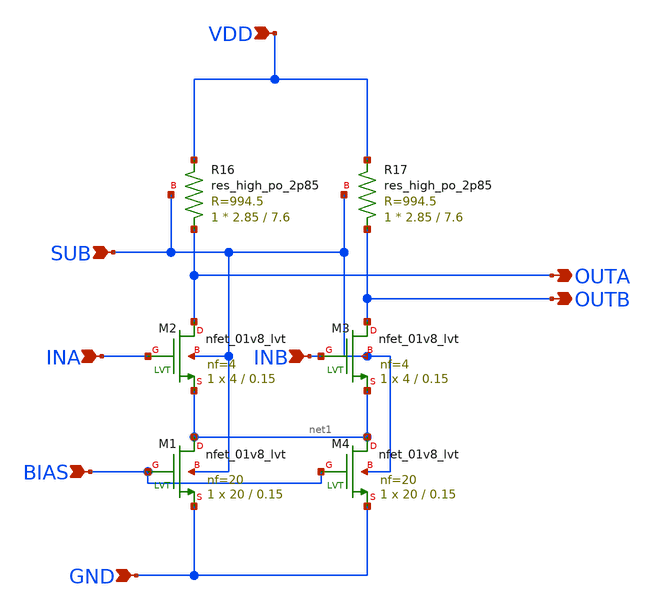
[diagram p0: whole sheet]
** sch_path: design/vco/5~10Ghiarachy_final/core_osc_amp.sch
**.subckt core_osc_amp INA INB BIAS GND VDD SUB OUTA OUTB
*.ipin INA
*.ipin INB
*.ipin BIAS
*.ipin GND
*.ipin VDD
*.ipin SUB
*.opin OUTA
*.opin OUTB
XM2 OUTA INA net1 SUB sky130_fd_pr__nfet_01v8_lvt L=0.15 W=4 nf=4 ad='int((nf+1)/2) * W/nf * 0.29' as='int((nf+2)/2) * W/nf * 0.29'
+ pd='2*int((nf+1)/2) * (W/nf + 0.29)' ps='2*int((nf+2)/2) * (W/nf + 0.29)' nrd='0.29 / W' nrs='0.29 / W'
+ sa=0 sb=0 sd=0 mult=1 m=1
XM3 OUTB INB net1 SUB sky130_fd_pr__nfet_01v8_lvt L=0.15 W=4 nf=4 ad='int((nf+1)/2) * W/nf * 0.29' as='int((nf+2)/2) * W/nf * 0.29'
+ pd='2*int((nf+1)/2) * (W/nf + 0.29)' ps='2*int((nf+2)/2) * (W/nf + 0.29)' nrd='0.29 / W' nrs='0.29 / W'
+ sa=0 sb=0 sd=0 mult=1 m=1
XM1 net1 BIAS GND SUB sky130_fd_pr__nfet_01v8_lvt L=0.15 W=20 nf=20 ad='int((nf+1)/2) * W/nf * 0.29'
+ as='int((nf+2)/2) * W/nf * 0.29' pd='2*int((nf+1)/2) * (W/nf + 0.29)' ps='2*int((nf+2)/2) * (W/nf + 0.29)'
+ nrd='0.29 / W' nrs='0.29 / W' sa=0 sb=0 sd=0 mult=1 m=1
XR16 OUTA VDD SUB sky130_fd_pr__res_high_po_2p85 L=7.6 mult=1 m=1
XR17 OUTB VDD SUB sky130_fd_pr__res_high_po_2p85 L=7.6 mult=1 m=1
XM4 net1 BIAS GND SUB sky130_fd_pr__nfet_01v8_lvt L=0.15 W=20 nf=20 ad='int((nf+1)/2) * W/nf * 0.29'
+ as='int((nf+2)/2) * W/nf * 0.29' pd='2*int((nf+1)/2) * (W/nf + 0.29)' ps='2*int((nf+2)/2) * (W/nf + 0.29)'
+ nrd='0.29 / W' nrs='0.29 / W' sa=0 sb=0 sd=0 mult=1 m=1
**.ends
.end
